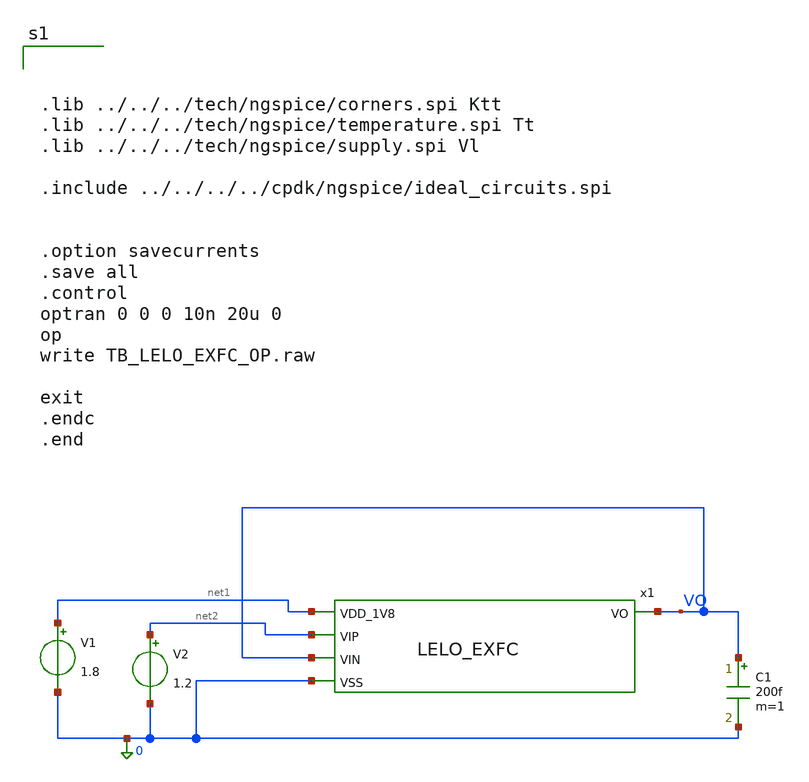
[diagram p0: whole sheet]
** sch_path: design/LELO_EXFC_SKY130A/TB_LELO_EXFC_OP.sch
**.subckt TB_LELO_EXFC_OP
x1 net1 VO net2 VO 0 LELO_EXFC
V1 net1 0 1.8
V2 net2 0 1.2
C1 VO 0 200f m=1
**** begin user architecture code



.lib ../../../tech/ngspice/corners.spi Ktt
.lib ../../../tech/ngspice/temperature.spi Tt
.lib ../../../tech/ngspice/supply.spi Vl

.include ../../../../cpdk/ngspice/ideal_circuits.spi


.option savecurrents
.save all
.control
optran 0 0 0 10n 20u 0
op
write TB_LELO_EXFC_OP.raw

exit
.endc
.end



**** end user architecture code
**.ends
.end
